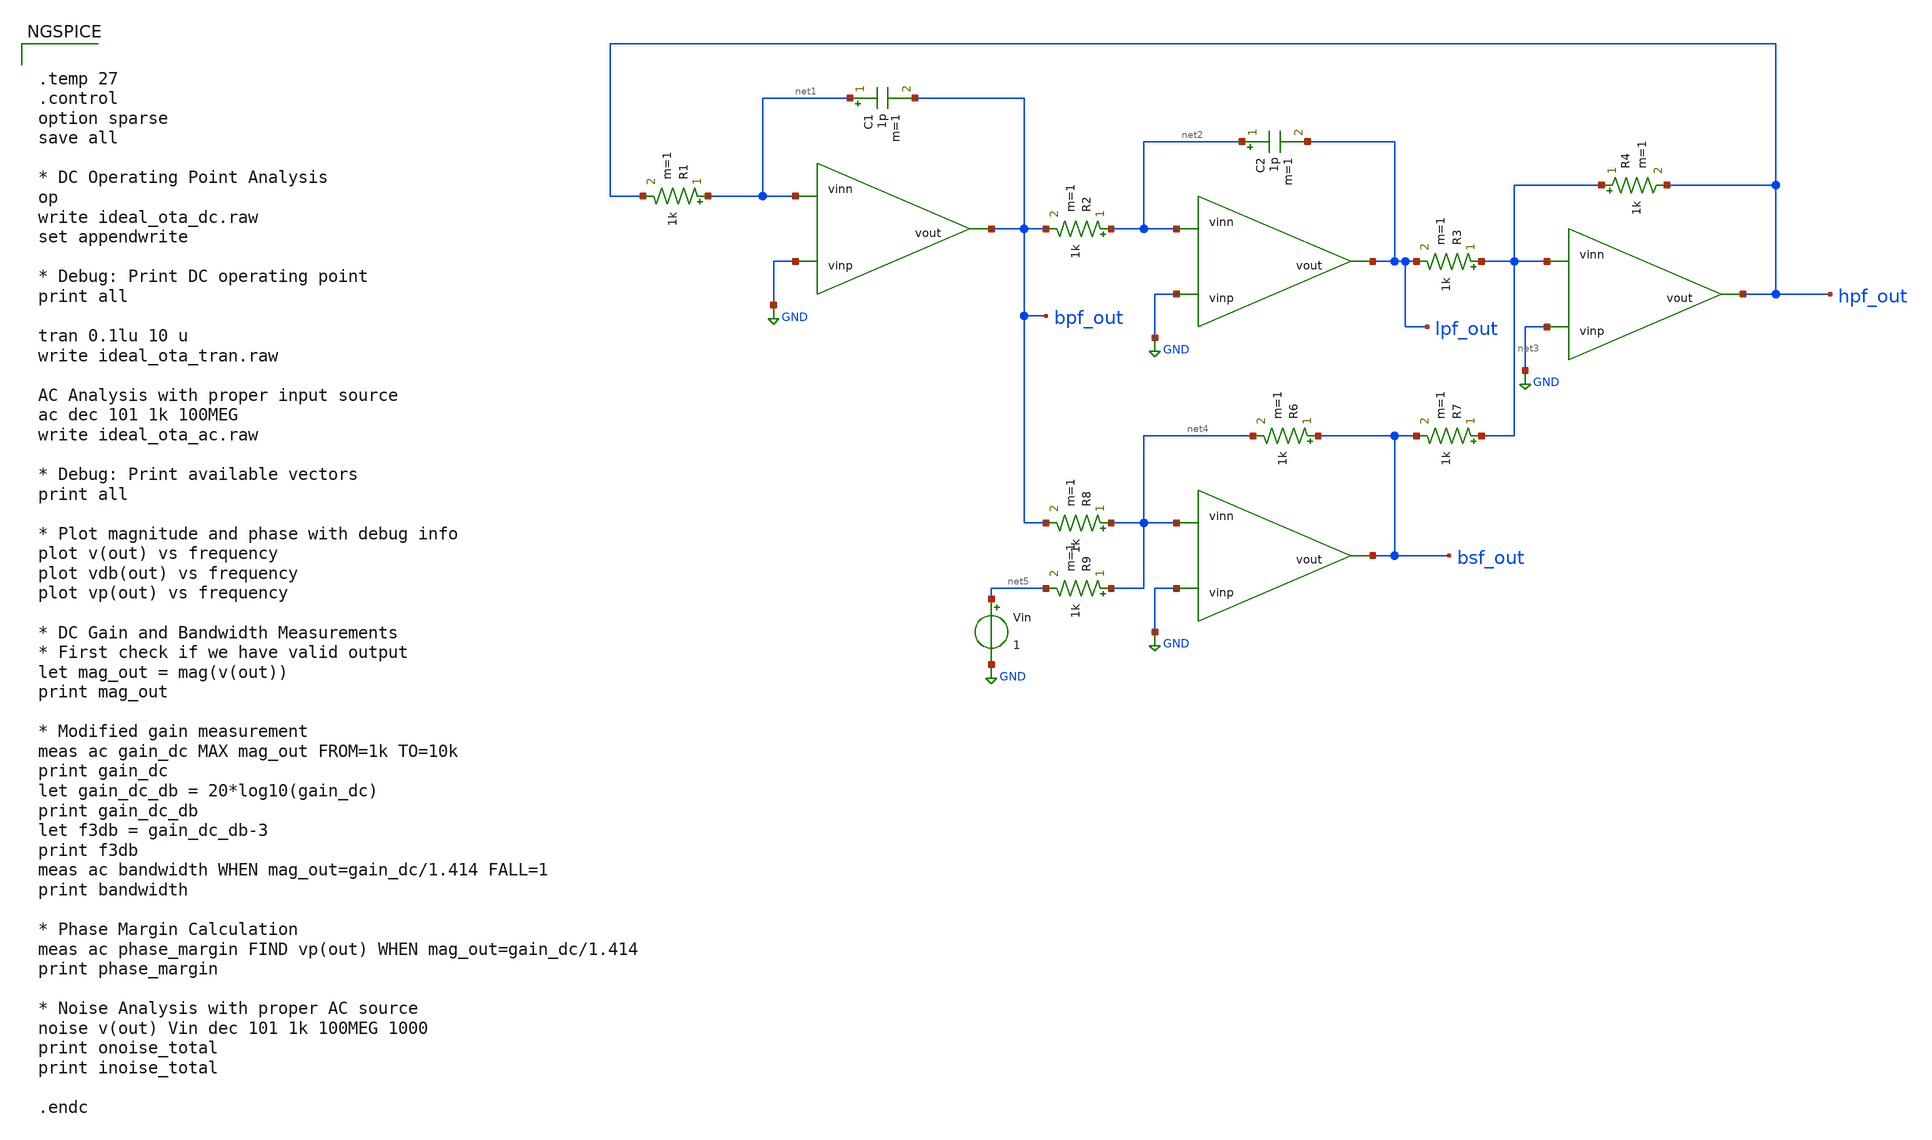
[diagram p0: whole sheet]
** sch_path: 2_Ideal_Cir/toplevel.sch
**.subckt toplevel
R1 net1 hpf_out 1k m=1
C1 net1 bpf_out 1p m=1
R2 net2 bpf_out 1k m=1
C2 net2 lpf_out 1p m=1
R3 net3 lpf_out 1k m=1
R4 net3 hpf_out 1k m=1
R6 bsf_out net4 1k m=1
R7 net3 bsf_out 1k m=1
R8 net4 bpf_out 1k m=1
R9 net4 net5 1k m=1
Vin net5 GND 1
**** begin user architecture code


.temp 27
.control
option sparse
save all

* DC Operating Point Analysis
op
write ideal_ota_dc.raw
set appendwrite

* Debug: Print DC operating point
print all

tran 0.1lu 10 u
write ideal_ota_tran.raw

AC Analysis with proper input source
ac dec 101 1k 100MEG
write ideal_ota_ac.raw

* Debug: Print available vectors
print all

* Plot magnitude and phase with debug info
plot v(out) vs frequency
plot vdb(out) vs frequency
plot vp(out) vs frequency

* DC Gain and Bandwidth Measurements
* First check if we have valid output
let mag_out = mag(v(out))
print mag_out

* Modified gain measurement
meas ac gain_dc MAX mag_out FROM=1k TO=10k
print gain_dc
let gain_dc_db = 20*log10(gain_dc)
print gain_dc_db
let f3db = gain_dc_db-3
print f3db
meas ac bandwidth WHEN mag_out=gain_dc/1.414 FALL=1
print bandwidth

* Phase Margin Calculation
meas ac phase_margin FIND vp(out) WHEN mag_out=gain_dc/1.414
print phase_margin

* Noise Analysis with proper AC source
noise v(out) Vin dec 101 1k 100MEG 1000
print onoise_total
print inoise_total

.endc


**** end user architecture code
**.ends
.GLOBAL GND
.end
